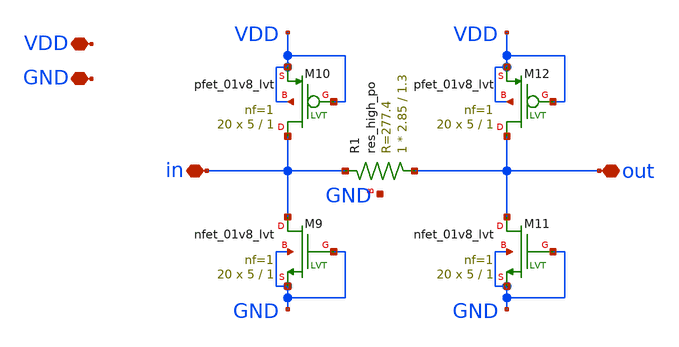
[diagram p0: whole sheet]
** sch_path: xschem/esd.sch
**.subckt esd in out VDD GND
*.iopin in
*.iopin out
*.iopin VDD
*.iopin GND
XM9 in GND GND GND sky130_fd_pr__nfet_01v8_lvt L=1 W=5 nf=1 ad='int((nf+1)/2) * W/nf * 0.29' as='int((nf+2)/2) * W/nf * 0.29'
+ pd='2*int((nf+1)/2) * (W/nf + 0.29)' ps='2*int((nf+2)/2) * (W/nf + 0.29)' nrd='0.29 / W' nrs='0.29 / W'
+ sa=0 sb=0 sd=0 mult=20 m=20
XM10 in VDD VDD VDD sky130_fd_pr__pfet_01v8_lvt L=1 W=5 nf=1 ad='int((nf+1)/2) * W/nf * 0.29' as='int((nf+2)/2) * W/nf * 0.29'
+ pd='2*int((nf+1)/2) * (W/nf + 0.29)' ps='2*int((nf+2)/2) * (W/nf + 0.29)' nrd='0.29 / W' nrs='0.29 / W'
+ sa=0 sb=0 sd=0 mult=20 m=20
XM11 out GND GND GND sky130_fd_pr__nfet_01v8_lvt L=1 W=5 nf=1 ad='int((nf+1)/2) * W/nf * 0.29' as='int((nf+2)/2) * W/nf * 0.29'
+ pd='2*int((nf+1)/2) * (W/nf + 0.29)' ps='2*int((nf+2)/2) * (W/nf + 0.29)' nrd='0.29 / W' nrs='0.29 / W'
+ sa=0 sb=0 sd=0 mult=20 m=20
XM12 out VDD VDD VDD sky130_fd_pr__pfet_01v8_lvt L=1 W=5 nf=1 ad='int((nf+1)/2) * W/nf * 0.29' as='int((nf+2)/2) * W/nf * 0.29'
+ pd='2*int((nf+1)/2) * (W/nf + 0.29)' ps='2*int((nf+2)/2) * (W/nf + 0.29)' nrd='0.29 / W' nrs='0.29 / W'
+ sa=0 sb=0 sd=0 mult=20 m=20
XR1 out in GND sky130_fd_pr__res_high_po W=2.85 L=1.3 mult=1 m=1
**.ends
.end
